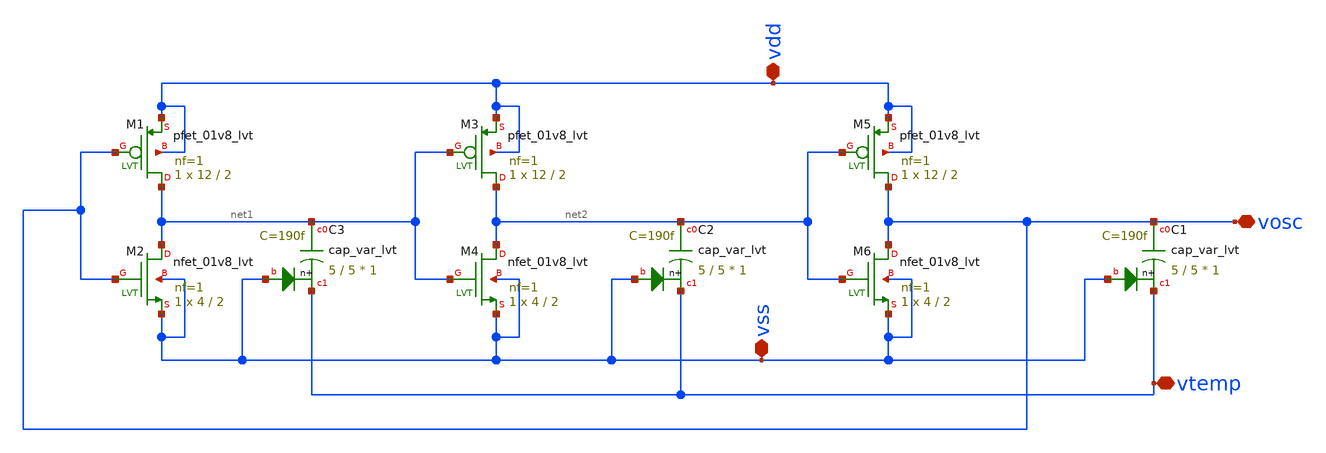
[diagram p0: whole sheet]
** sch_path: XSCHEM/For_Layout/ring_oscillator.sch
**.subckt ring_oscillator vtemp vss vdd vosc
*.iopin vtemp
*.iopin vss
*.iopin vdd
*.iopin vosc
XM1 net1 vosc vdd vdd sky130_fd_pr__pfet_01v8_lvt L=2 W=12 nf=1 ad='int((nf+1)/2) * W/nf * 0.29' as='int((nf+2)/2) * W/nf * 0.29'
+ pd='2*int((nf+1)/2) * (W/nf + 0.29)' ps='2*int((nf+2)/2) * (W/nf + 0.29)' nrd='0.29 / W' nrs='0.29 / W'
+ sa=0 sb=0 sd=0 mult=1 m=1
XM2 net1 vosc vss vss sky130_fd_pr__nfet_01v8_lvt L=2 W=4 nf=1 ad='int((nf+1)/2) * W/nf * 0.29' as='int((nf+2)/2) * W/nf * 0.29'
+ pd='2*int((nf+1)/2) * (W/nf + 0.29)' ps='2*int((nf+2)/2) * (W/nf + 0.29)' nrd='0.29 / W' nrs='0.29 / W'
+ sa=0 sb=0 sd=0 mult=1 m=1
XM3 net2 net1 vdd vdd sky130_fd_pr__pfet_01v8_lvt L=2 W=12 nf=1 ad='int((nf+1)/2) * W/nf * 0.29' as='int((nf+2)/2) * W/nf * 0.29'
+ pd='2*int((nf+1)/2) * (W/nf + 0.29)' ps='2*int((nf+2)/2) * (W/nf + 0.29)' nrd='0.29 / W' nrs='0.29 / W'
+ sa=0 sb=0 sd=0 mult=1 m=1
XM4 net2 net1 vss vss sky130_fd_pr__nfet_01v8_lvt L=2 W=4 nf=1 ad='int((nf+1)/2) * W/nf * 0.29' as='int((nf+2)/2) * W/nf * 0.29'
+ pd='2*int((nf+1)/2) * (W/nf + 0.29)' ps='2*int((nf+2)/2) * (W/nf + 0.29)' nrd='0.29 / W' nrs='0.29 / W'
+ sa=0 sb=0 sd=0 mult=1 m=1
XM5 vosc net2 vdd vdd sky130_fd_pr__pfet_01v8_lvt L=2 W=12 nf=1 ad='int((nf+1)/2) * W/nf * 0.29' as='int((nf+2)/2) * W/nf * 0.29'
+ pd='2*int((nf+1)/2) * (W/nf + 0.29)' ps='2*int((nf+2)/2) * (W/nf + 0.29)' nrd='0.29 / W' nrs='0.29 / W'
+ sa=0 sb=0 sd=0 mult=1 m=1
XM6 vosc net2 vss vss sky130_fd_pr__nfet_01v8_lvt L=2 W=4 nf=1 ad='int((nf+1)/2) * W/nf * 0.29' as='int((nf+2)/2) * W/nf * 0.29'
+ pd='2*int((nf+1)/2) * (W/nf + 0.29)' ps='2*int((nf+2)/2) * (W/nf + 0.29)' nrd='0.29 / W' nrs='0.29 / W'
+ sa=0 sb=0 sd=0 mult=1 m=1
XC1 vosc vtemp vss sky130_fd_pr__cap_var_lvt W=5 L=5 VM=1 m=1
XC2 net2 vtemp vss sky130_fd_pr__cap_var_lvt W=5 L=5 VM=1 m=1
XC3 net1 vtemp vss sky130_fd_pr__cap_var_lvt W=5 L=5 VM=1 m=1
**.ends
.end
